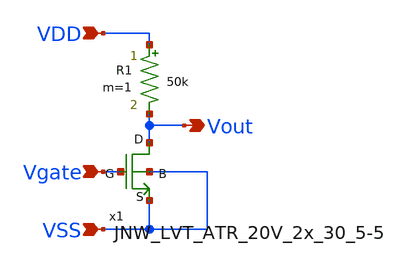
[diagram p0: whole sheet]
** sch_path: design/THESIS_EXP_RO_INVERTER_SKY130A/INV_ZVT_R.sch
**.subckt INV_ZVT_R VDD VSS Vgate Vout
*.ipin VDD
*.ipin VSS
*.ipin Vgate
*.opin Vout
R1 VDD Vout 50k m=1
x1 Vout Vgate VSS VSS JNW_LVT_ATR_20V_2x_30_5-5
**.ends

* expanding   symbol:  JNW_ZVT_ATR_SKY130A/JNW_LVT_ATR_20V_2x_30_5-5.sym # of pins=4
** sym_path: design/JNW_ZVT_ATR_SKY130A/JNW_LVT_ATR_20V_2x_30_5-5.sym
** sch_path: design/JNW_ZVT_ATR_SKY130A/JNW_LVT_ATR_20V_2x_30_5-5.sch
.subckt JNW_LVT_ATR_20V_2x_30_5-5 D G S B
*.iopin D
*.iopin G
*.iopin S
*.iopin B
XM1 D G S B sky130_fd_pr__nfet_20v0_zvt W=30 L=5.5 m=2
.ends

.end
